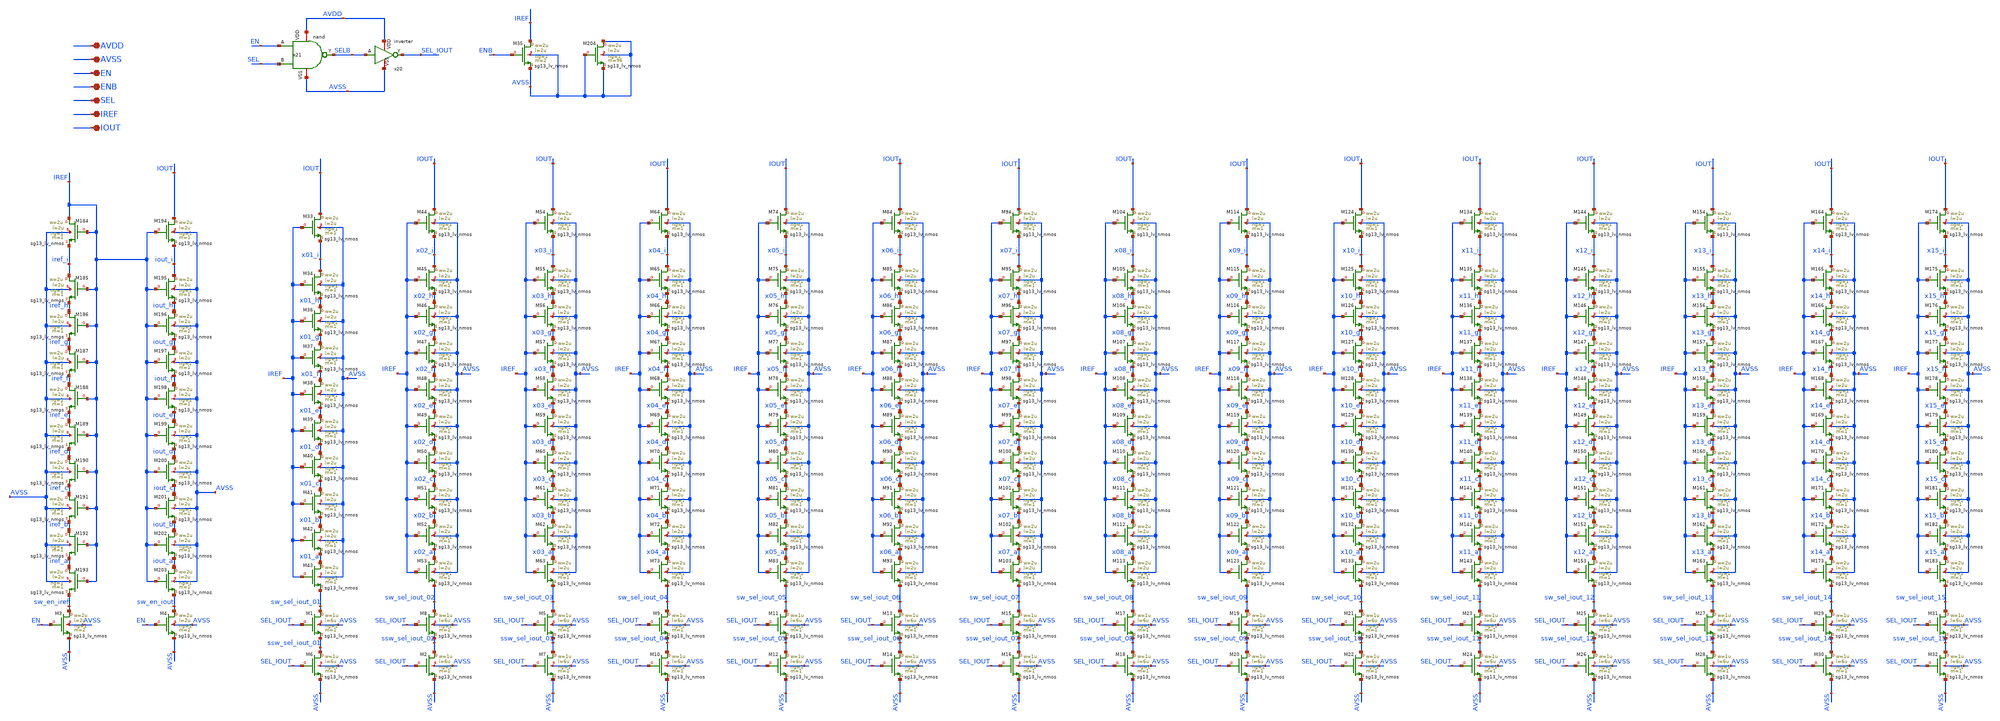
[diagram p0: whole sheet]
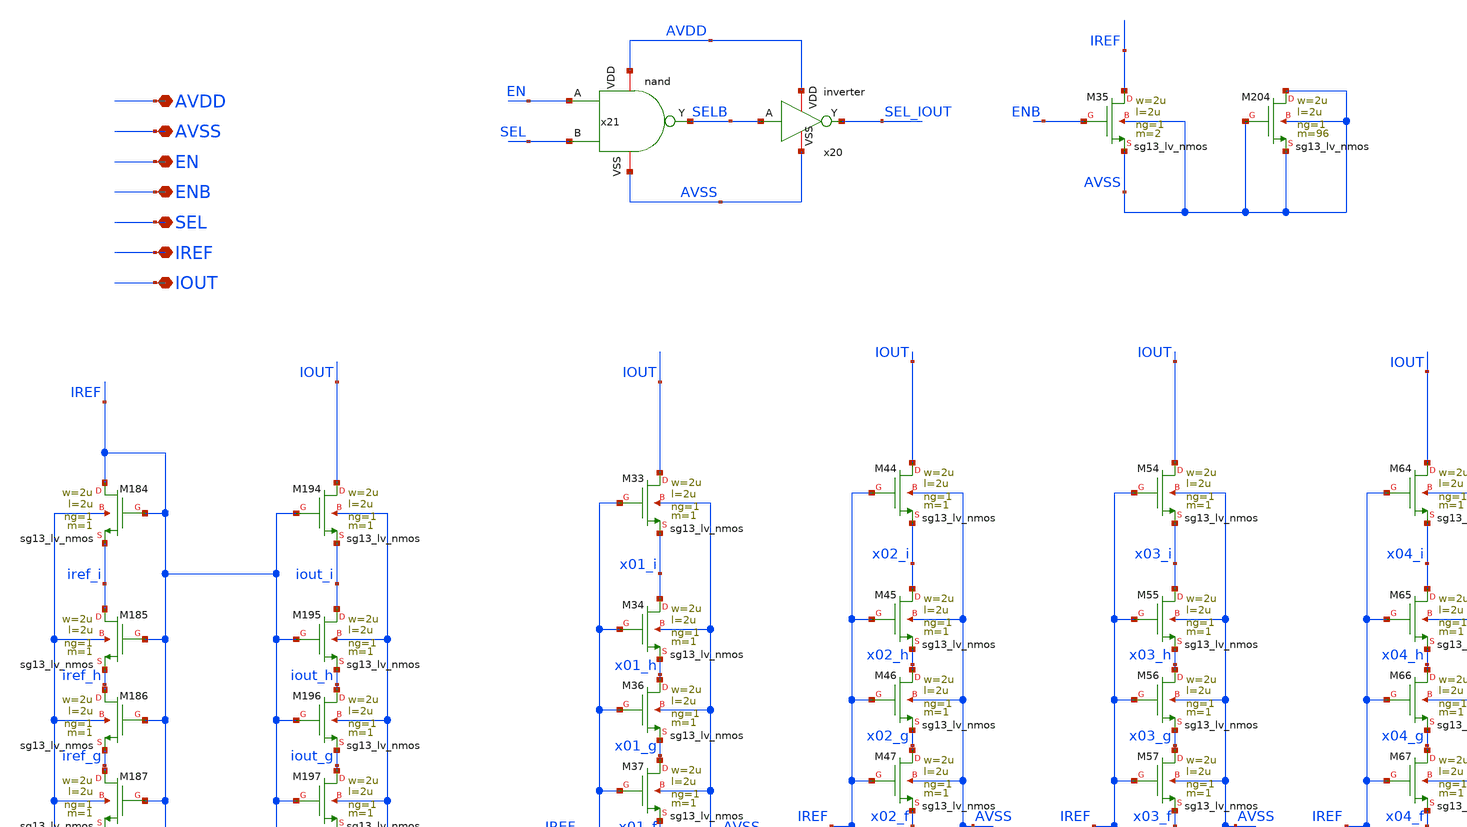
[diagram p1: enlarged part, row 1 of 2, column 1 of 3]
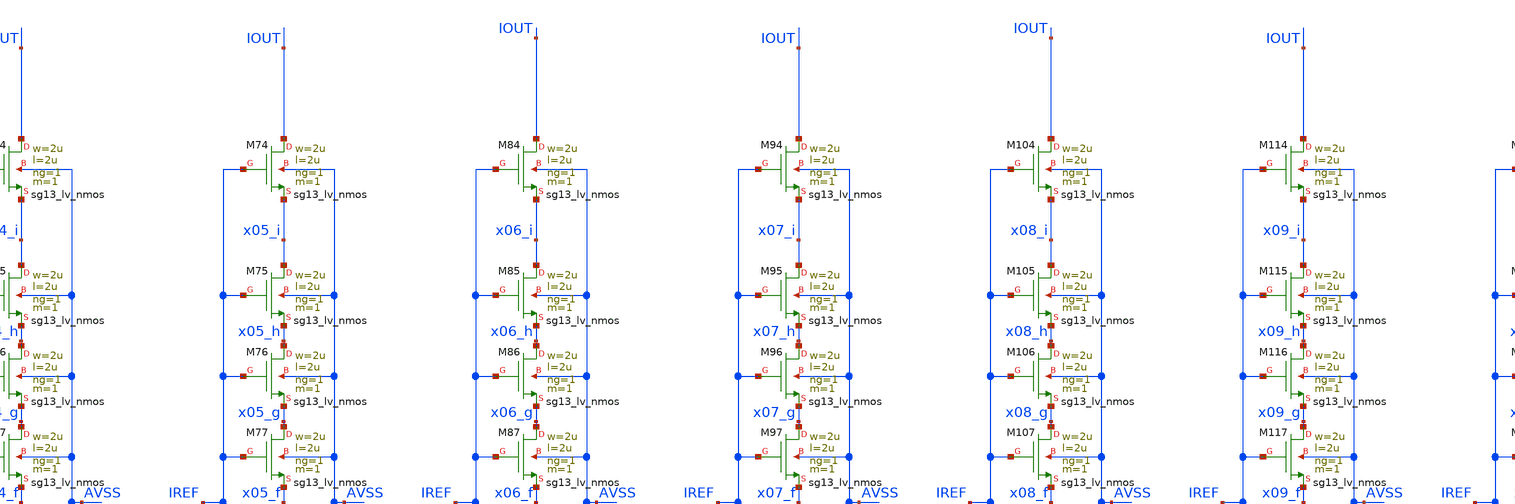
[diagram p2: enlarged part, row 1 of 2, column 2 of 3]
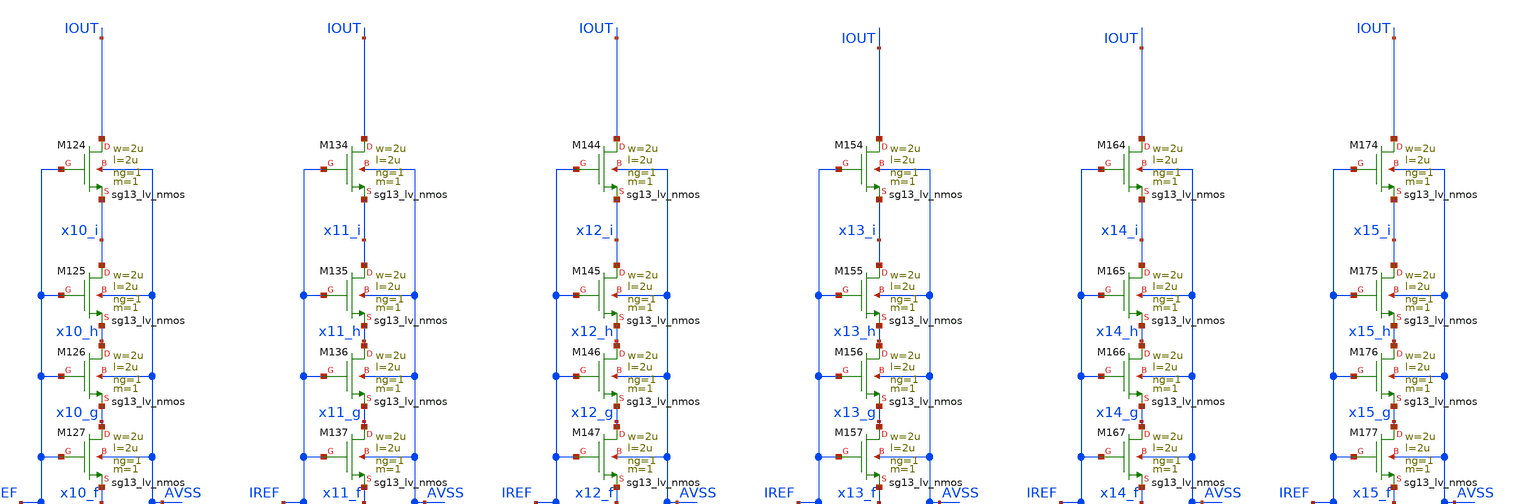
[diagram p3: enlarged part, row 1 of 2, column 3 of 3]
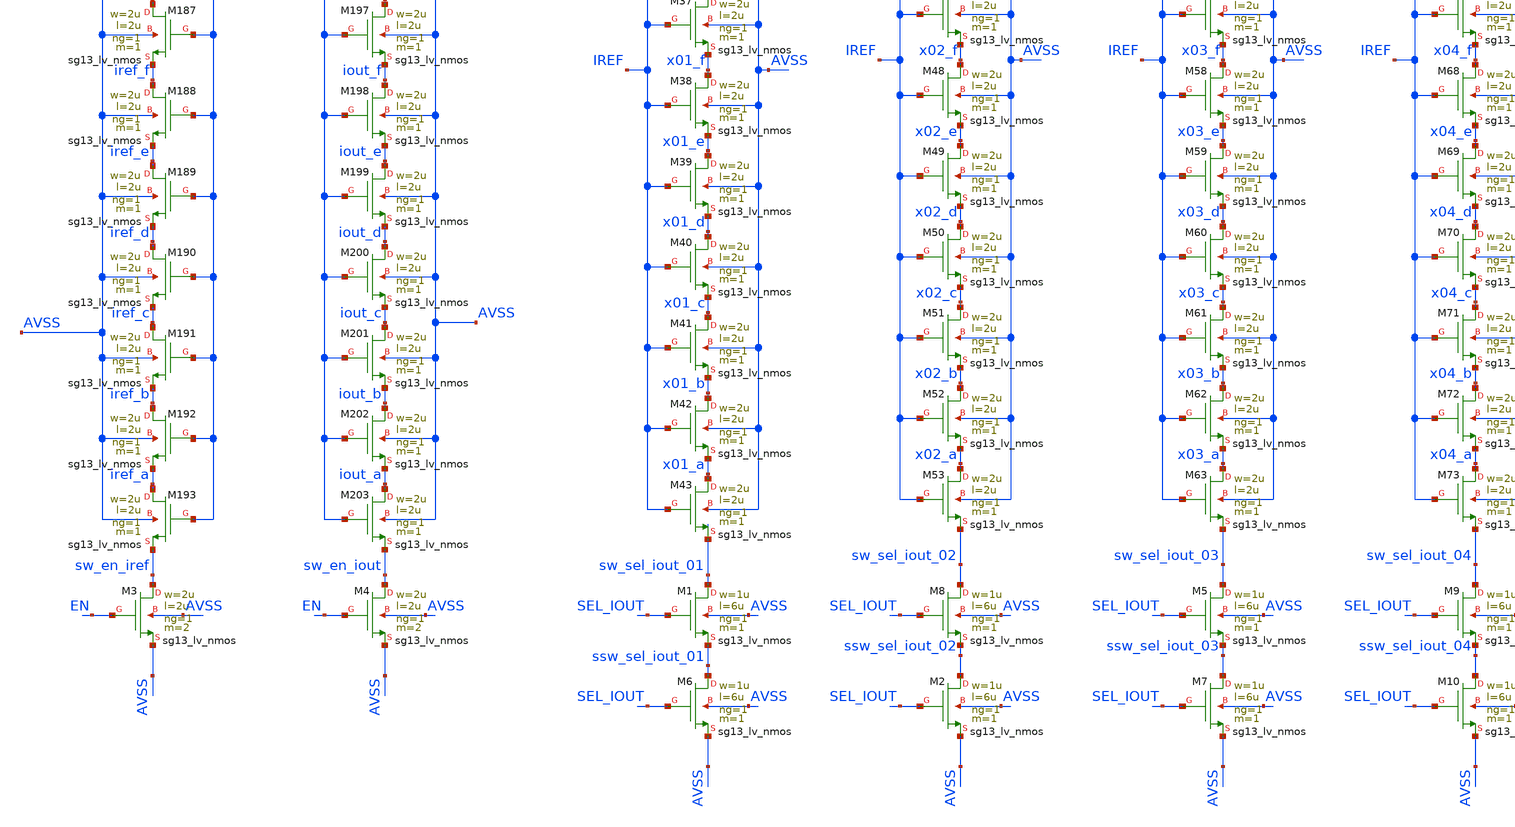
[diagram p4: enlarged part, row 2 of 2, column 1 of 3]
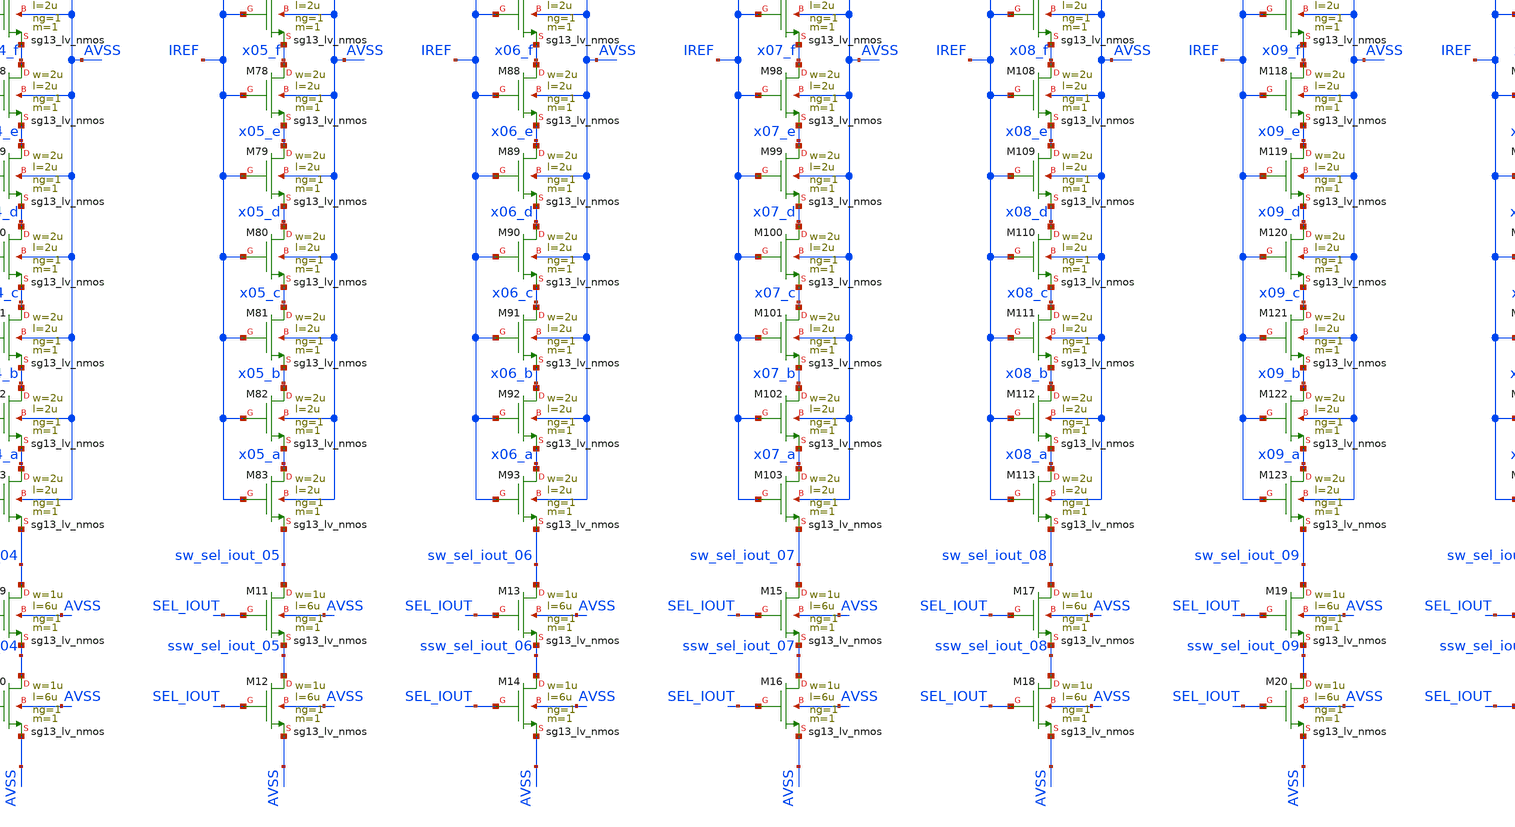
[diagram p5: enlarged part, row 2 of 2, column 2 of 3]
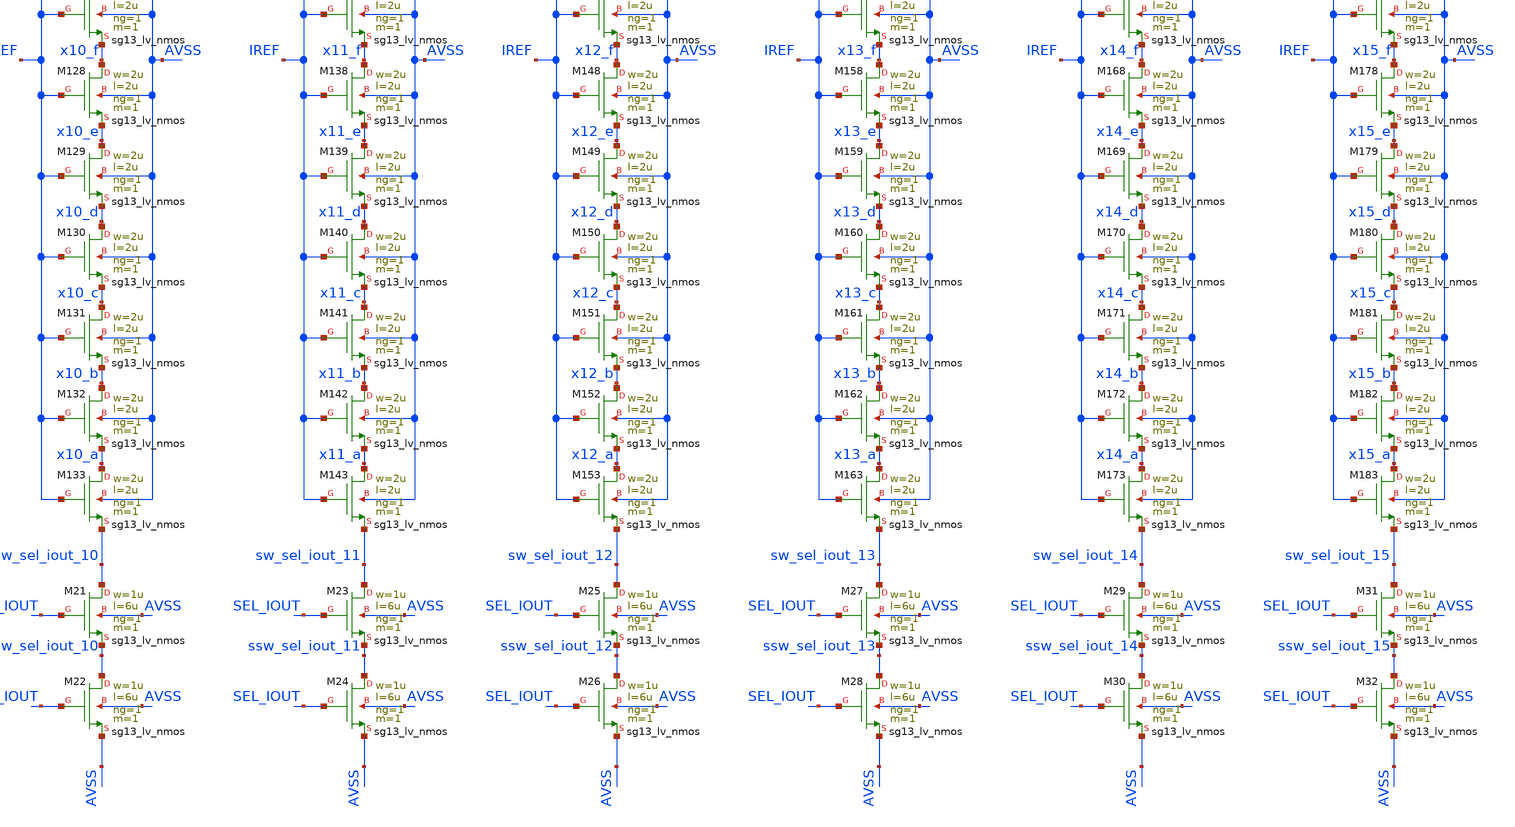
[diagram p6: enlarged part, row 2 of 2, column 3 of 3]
** sch_path: current_generator/analog/DAC/schematics/current_mirror.sch
**.subckt current_mirror AVDD AVSS EN ENB SEL IREF IOUT
*.iopin AVDD
*.iopin AVSS
*.iopin EN
*.iopin ENB
*.iopin SEL
*.iopin IREF
*.iopin IOUT
XM3 sw_en_iref EN AVSS AVSS sg13_lv_nmos w=2u l=2u ng=1 m=2 mm_ok=1
XM4 sw_en_iout EN AVSS AVSS sg13_lv_nmos w=2u l=2u ng=1 m=2 mm_ok=1
XM8 sw_sel_iout_02 SEL_IOUT ssw_sel_iout_02 AVSS sg13_lv_nmos w=1u l=6u ng=1 m=1 mm_ok=1
XM35 IREF ENB AVSS AVSS sg13_lv_nmos w=2u l=2u ng=1 m=2 mm_ok=1
XM2 ssw_sel_iout_02 SEL_IOUT AVSS AVSS sg13_lv_nmos w=1u l=6u ng=1 m=1 mm_ok=1
XM1 sw_sel_iout_01 SEL_IOUT ssw_sel_iout_01 AVSS sg13_lv_nmos w=1u l=6u ng=1 m=1 mm_ok=1
XM6 ssw_sel_iout_01 SEL_IOUT AVSS AVSS sg13_lv_nmos w=1u l=6u ng=1 m=1 mm_ok=1
XM5 sw_sel_iout_03 SEL_IOUT ssw_sel_iout_03 AVSS sg13_lv_nmos w=1u l=6u ng=1 m=1 mm_ok=1
XM7 ssw_sel_iout_03 SEL_IOUT AVSS AVSS sg13_lv_nmos w=1u l=6u ng=1 m=1 mm_ok=1
XM9 sw_sel_iout_04 SEL_IOUT ssw_sel_iout_04 AVSS sg13_lv_nmos w=1u l=6u ng=1 m=1 mm_ok=1
XM10 ssw_sel_iout_04 SEL_IOUT AVSS AVSS sg13_lv_nmos w=1u l=6u ng=1 m=1 mm_ok=1
XM11 sw_sel_iout_05 SEL_IOUT ssw_sel_iout_05 AVSS sg13_lv_nmos w=1u l=6u ng=1 m=1 mm_ok=1
XM12 ssw_sel_iout_05 SEL_IOUT AVSS AVSS sg13_lv_nmos w=1u l=6u ng=1 m=1 mm_ok=1
XM13 sw_sel_iout_06 SEL_IOUT ssw_sel_iout_06 AVSS sg13_lv_nmos w=1u l=6u ng=1 m=1 mm_ok=1
XM14 ssw_sel_iout_06 SEL_IOUT AVSS AVSS sg13_lv_nmos w=1u l=6u ng=1 m=1 mm_ok=1
XM15 sw_sel_iout_07 SEL_IOUT ssw_sel_iout_07 AVSS sg13_lv_nmos w=1u l=6u ng=1 m=1 mm_ok=1
XM16 ssw_sel_iout_07 SEL_IOUT AVSS AVSS sg13_lv_nmos w=1u l=6u ng=1 m=1 mm_ok=1
XM17 sw_sel_iout_08 SEL_IOUT ssw_sel_iout_08 AVSS sg13_lv_nmos w=1u l=6u ng=1 m=1 mm_ok=1
XM18 ssw_sel_iout_08 SEL_IOUT AVSS AVSS sg13_lv_nmos w=1u l=6u ng=1 m=1 mm_ok=1
XM19 sw_sel_iout_09 SEL_IOUT ssw_sel_iout_09 AVSS sg13_lv_nmos w=1u l=6u ng=1 m=1 mm_ok=1
XM20 ssw_sel_iout_09 SEL_IOUT AVSS AVSS sg13_lv_nmos w=1u l=6u ng=1 m=1 mm_ok=1
XM21 sw_sel_iout_10 SEL_IOUT ssw_sel_iout_10 AVSS sg13_lv_nmos w=1u l=6u ng=1 m=1 mm_ok=1
XM22 ssw_sel_iout_10 SEL_IOUT AVSS AVSS sg13_lv_nmos w=1u l=6u ng=1 m=1 mm_ok=1
XM23 sw_sel_iout_11 SEL_IOUT ssw_sel_iout_11 AVSS sg13_lv_nmos w=1u l=6u ng=1 m=1 mm_ok=1
XM24 ssw_sel_iout_11 SEL_IOUT AVSS AVSS sg13_lv_nmos w=1u l=6u ng=1 m=1 mm_ok=1
XM25 sw_sel_iout_12 SEL_IOUT ssw_sel_iout_12 AVSS sg13_lv_nmos w=1u l=6u ng=1 m=1 mm_ok=1
XM26 ssw_sel_iout_12 SEL_IOUT AVSS AVSS sg13_lv_nmos w=1u l=6u ng=1 m=1 mm_ok=1
XM27 sw_sel_iout_13 SEL_IOUT ssw_sel_iout_13 AVSS sg13_lv_nmos w=1u l=6u ng=1 m=1 mm_ok=1
XM28 ssw_sel_iout_13 SEL_IOUT AVSS AVSS sg13_lv_nmos w=1u l=6u ng=1 m=1 mm_ok=1
XM29 sw_sel_iout_14 SEL_IOUT ssw_sel_iout_14 AVSS sg13_lv_nmos w=1u l=6u ng=1 m=1 mm_ok=1
XM30 ssw_sel_iout_14 SEL_IOUT AVSS AVSS sg13_lv_nmos w=1u l=6u ng=1 m=1 mm_ok=1
XM31 sw_sel_iout_15 SEL_IOUT ssw_sel_iout_15 AVSS sg13_lv_nmos w=1u l=6u ng=1 m=1 mm_ok=1
XM32 ssw_sel_iout_15 SEL_IOUT AVSS AVSS sg13_lv_nmos w=1u l=6u ng=1 m=1 mm_ok=1
x20 SELB SEL_IOUT AVDD AVSS inverter
x21 AVDD AVSS EN SEL SELB nand
XM33 IOUT IREF x01_i AVSS sg13_lv_nmos w=2u l=2u ng=1 m=1 mm_ok=1
XM34 x01_i IREF x01_h AVSS sg13_lv_nmos w=2u l=2u ng=1 m=1 mm_ok=1
XM36 x01_h IREF x01_g AVSS sg13_lv_nmos w=2u l=2u ng=1 m=1 mm_ok=1
XM37 x01_g IREF x01_f AVSS sg13_lv_nmos w=2u l=2u ng=1 m=1 mm_ok=1
XM38 x01_f IREF x01_e AVSS sg13_lv_nmos w=2u l=2u ng=1 m=1 mm_ok=1
XM39 x01_e IREF x01_d AVSS sg13_lv_nmos w=2u l=2u ng=1 m=1 mm_ok=1
XM40 x01_d IREF x01_c AVSS sg13_lv_nmos w=2u l=2u ng=1 m=1 mm_ok=1
XM41 x01_c IREF x01_b AVSS sg13_lv_nmos w=2u l=2u ng=1 m=1 mm_ok=1
XM42 x01_b IREF x01_a AVSS sg13_lv_nmos w=2u l=2u ng=1 m=1 mm_ok=1
XM43 x01_a IREF sw_sel_iout_01 AVSS sg13_lv_nmos w=2u l=2u ng=1 m=1 mm_ok=1
XM44 IOUT IREF x02_i AVSS sg13_lv_nmos w=2u l=2u ng=1 m=1 mm_ok=1
XM45 x02_i IREF x02_h AVSS sg13_lv_nmos w=2u l=2u ng=1 m=1 mm_ok=1
XM46 x02_h IREF x02_g AVSS sg13_lv_nmos w=2u l=2u ng=1 m=1 mm_ok=1
XM47 x02_g IREF x02_f AVSS sg13_lv_nmos w=2u l=2u ng=1 m=1 mm_ok=1
XM48 x02_f IREF x02_e AVSS sg13_lv_nmos w=2u l=2u ng=1 m=1 mm_ok=1
XM49 x02_e IREF x02_d AVSS sg13_lv_nmos w=2u l=2u ng=1 m=1 mm_ok=1
XM50 x02_d IREF x02_c AVSS sg13_lv_nmos w=2u l=2u ng=1 m=1 mm_ok=1
XM51 x02_c IREF x02_b AVSS sg13_lv_nmos w=2u l=2u ng=1 m=1 mm_ok=1
XM52 x02_b IREF x02_a AVSS sg13_lv_nmos w=2u l=2u ng=1 m=1 mm_ok=1
XM53 x02_a IREF sw_sel_iout_02 AVSS sg13_lv_nmos w=2u l=2u ng=1 m=1 mm_ok=1
XM54 IOUT IREF x03_i AVSS sg13_lv_nmos w=2u l=2u ng=1 m=1 mm_ok=1
XM55 x03_i IREF x03_h AVSS sg13_lv_nmos w=2u l=2u ng=1 m=1 mm_ok=1
XM56 x03_h IREF x03_g AVSS sg13_lv_nmos w=2u l=2u ng=1 m=1 mm_ok=1
XM57 x03_g IREF x03_f AVSS sg13_lv_nmos w=2u l=2u ng=1 m=1 mm_ok=1
XM58 x03_f IREF x03_e AVSS sg13_lv_nmos w=2u l=2u ng=1 m=1 mm_ok=1
XM59 x03_e IREF x03_d AVSS sg13_lv_nmos w=2u l=2u ng=1 m=1 mm_ok=1
XM60 x03_d IREF x03_c AVSS sg13_lv_nmos w=2u l=2u ng=1 m=1 mm_ok=1
XM61 x03_c IREF x03_b AVSS sg13_lv_nmos w=2u l=2u ng=1 m=1 mm_ok=1
XM62 x03_b IREF x03_a AVSS sg13_lv_nmos w=2u l=2u ng=1 m=1 mm_ok=1
XM63 x03_a IREF sw_sel_iout_03 AVSS sg13_lv_nmos w=2u l=2u ng=1 m=1 mm_ok=1
XM64 IOUT IREF x04_i AVSS sg13_lv_nmos w=2u l=2u ng=1 m=1 mm_ok=1
XM65 x04_i IREF x04_h AVSS sg13_lv_nmos w=2u l=2u ng=1 m=1 mm_ok=1
XM66 x04_h IREF x04_g AVSS sg13_lv_nmos w=2u l=2u ng=1 m=1 mm_ok=1
XM67 x04_g IREF x04_f AVSS sg13_lv_nmos w=2u l=2u ng=1 m=1 mm_ok=1
XM68 x04_f IREF x04_e AVSS sg13_lv_nmos w=2u l=2u ng=1 m=1 mm_ok=1
XM69 x04_e IREF x04_d AVSS sg13_lv_nmos w=2u l=2u ng=1 m=1 mm_ok=1
XM70 x04_d IREF x04_c AVSS sg13_lv_nmos w=2u l=2u ng=1 m=1 mm_ok=1
XM71 x04_c IREF x04_b AVSS sg13_lv_nmos w=2u l=2u ng=1 m=1 mm_ok=1
XM72 x04_b IREF x04_a AVSS sg13_lv_nmos w=2u l=2u ng=1 m=1 mm_ok=1
XM73 x04_a IREF sw_sel_iout_04 AVSS sg13_lv_nmos w=2u l=2u ng=1 m=1 mm_ok=1
XM74 IOUT IREF x05_i AVSS sg13_lv_nmos w=2u l=2u ng=1 m=1 mm_ok=1
XM75 x05_i IREF x05_h AVSS sg13_lv_nmos w=2u l=2u ng=1 m=1 mm_ok=1
XM76 x05_h IREF x05_g AVSS sg13_lv_nmos w=2u l=2u ng=1 m=1 mm_ok=1
XM77 x05_g IREF x05_f AVSS sg13_lv_nmos w=2u l=2u ng=1 m=1 mm_ok=1
XM78 x05_f IREF x05_e AVSS sg13_lv_nmos w=2u l=2u ng=1 m=1 mm_ok=1
XM79 x05_e IREF x05_d AVSS sg13_lv_nmos w=2u l=2u ng=1 m=1 mm_ok=1
XM80 x05_d IREF x05_c AVSS sg13_lv_nmos w=2u l=2u ng=1 m=1 mm_ok=1
XM81 x05_c IREF x05_b AVSS sg13_lv_nmos w=2u l=2u ng=1 m=1 mm_ok=1
XM82 x05_b IREF x05_a AVSS sg13_lv_nmos w=2u l=2u ng=1 m=1 mm_ok=1
XM83 x05_a IREF sw_sel_iout_05 AVSS sg13_lv_nmos w=2u l=2u ng=1 m=1 mm_ok=1
XM84 IOUT IREF x06_i AVSS sg13_lv_nmos w=2u l=2u ng=1 m=1 mm_ok=1
XM85 x06_i IREF x06_h AVSS sg13_lv_nmos w=2u l=2u ng=1 m=1 mm_ok=1
XM86 x06_h IREF x06_g AVSS sg13_lv_nmos w=2u l=2u ng=1 m=1 mm_ok=1
XM87 x06_g IREF x06_f AVSS sg13_lv_nmos w=2u l=2u ng=1 m=1 mm_ok=1
XM88 x06_f IREF x06_e AVSS sg13_lv_nmos w=2u l=2u ng=1 m=1 mm_ok=1
XM89 x06_e IREF x06_d AVSS sg13_lv_nmos w=2u l=2u ng=1 m=1 mm_ok=1
XM90 x06_d IREF x06_c AVSS sg13_lv_nmos w=2u l=2u ng=1 m=1 mm_ok=1
XM91 x06_c IREF x06_b AVSS sg13_lv_nmos w=2u l=2u ng=1 m=1 mm_ok=1
XM92 x06_b IREF x06_a AVSS sg13_lv_nmos w=2u l=2u ng=1 m=1 mm_ok=1
XM93 x06_a IREF sw_sel_iout_06 AVSS sg13_lv_nmos w=2u l=2u ng=1 m=1 mm_ok=1
XM94 IOUT IREF x07_i AVSS sg13_lv_nmos w=2u l=2u ng=1 m=1 mm_ok=1
XM95 x07_i IREF x07_h AVSS sg13_lv_nmos w=2u l=2u ng=1 m=1 mm_ok=1
XM96 x07_h IREF x07_g AVSS sg13_lv_nmos w=2u l=2u ng=1 m=1 mm_ok=1
XM97 x07_g IREF x07_f AVSS sg13_lv_nmos w=2u l=2u ng=1 m=1 mm_ok=1
XM98 x07_f IREF x07_e AVSS sg13_lv_nmos w=2u l=2u ng=1 m=1 mm_ok=1
XM99 x07_e IREF x07_d AVSS sg13_lv_nmos w=2u l=2u ng=1 m=1 mm_ok=1
XM100 x07_d IREF x07_c AVSS sg13_lv_nmos w=2u l=2u ng=1 m=1 mm_ok=1
XM101 x07_c IREF x07_b AVSS sg13_lv_nmos w=2u l=2u ng=1 m=1 mm_ok=1
XM102 x07_b IREF x07_a AVSS sg13_lv_nmos w=2u l=2u ng=1 m=1 mm_ok=1
XM103 x07_a IREF sw_sel_iout_07 AVSS sg13_lv_nmos w=2u l=2u ng=1 m=1 mm_ok=1
XM104 IOUT IREF x08_i AVSS sg13_lv_nmos w=2u l=2u ng=1 m=1 mm_ok=1
XM105 x08_i IREF x08_h AVSS sg13_lv_nmos w=2u l=2u ng=1 m=1 mm_ok=1
XM106 x08_h IREF x08_g AVSS sg13_lv_nmos w=2u l=2u ng=1 m=1 mm_ok=1
XM107 x08_g IREF x08_f AVSS sg13_lv_nmos w=2u l=2u ng=1 m=1 mm_ok=1
XM108 x08_f IREF x08_e AVSS sg13_lv_nmos w=2u l=2u ng=1 m=1 mm_ok=1
XM109 x08_e IREF x08_d AVSS sg13_lv_nmos w=2u l=2u ng=1 m=1 mm_ok=1
XM110 x08_d IREF x08_c AVSS sg13_lv_nmos w=2u l=2u ng=1 m=1 mm_ok=1
XM111 x08_c IREF x08_b AVSS sg13_lv_nmos w=2u l=2u ng=1 m=1 mm_ok=1
XM112 x08_b IREF x08_a AVSS sg13_lv_nmos w=2u l=2u ng=1 m=1 mm_ok=1
XM113 x08_a IREF sw_sel_iout_08 AVSS sg13_lv_nmos w=2u l=2u ng=1 m=1 mm_ok=1
XM114 IOUT IREF x09_i AVSS sg13_lv_nmos w=2u l=2u ng=1 m=1 mm_ok=1
XM115 x09_i IREF x09_h AVSS sg13_lv_nmos w=2u l=2u ng=1 m=1 mm_ok=1
XM116 x09_h IREF x09_g AVSS sg13_lv_nmos w=2u l=2u ng=1 m=1 mm_ok=1
XM117 x09_g IREF x09_f AVSS sg13_lv_nmos w=2u l=2u ng=1 m=1 mm_ok=1
XM118 x09_f IREF x09_e AVSS sg13_lv_nmos w=2u l=2u ng=1 m=1 mm_ok=1
XM119 x09_e IREF x09_d AVSS sg13_lv_nmos w=2u l=2u ng=1 m=1 mm_ok=1
XM120 x09_d IREF x09_c AVSS sg13_lv_nmos w=2u l=2u ng=1 m=1 mm_ok=1
XM121 x09_c IREF x09_b AVSS sg13_lv_nmos w=2u l=2u ng=1 m=1 mm_ok=1
XM122 x09_b IREF x09_a AVSS sg13_lv_nmos w=2u l=2u ng=1 m=1 mm_ok=1
XM123 x09_a IREF sw_sel_iout_09 AVSS sg13_lv_nmos w=2u l=2u ng=1 m=1 mm_ok=1
XM124 IOUT IREF x10_i AVSS sg13_lv_nmos w=2u l=2u ng=1 m=1 mm_ok=1
XM125 x10_i IREF x10_h AVSS sg13_lv_nmos w=2u l=2u ng=1 m=1 mm_ok=1
XM126 x10_h IREF x10_g AVSS sg13_lv_nmos w=2u l=2u ng=1 m=1 mm_ok=1
XM127 x10_g IREF x10_f AVSS sg13_lv_nmos w=2u l=2u ng=1 m=1 mm_ok=1
XM128 x10_f IREF x10_e AVSS sg13_lv_nmos w=2u l=2u ng=1 m=1 mm_ok=1
XM129 x10_e IREF x10_d AVSS sg13_lv_nmos w=2u l=2u ng=1 m=1 mm_ok=1
XM130 x10_d IREF x10_c AVSS sg13_lv_nmos w=2u l=2u ng=1 m=1 mm_ok=1
XM131 x10_c IREF x10_b AVSS sg13_lv_nmos w=2u l=2u ng=1 m=1 mm_ok=1
XM132 x10_b IREF x10_a AVSS sg13_lv_nmos w=2u l=2u ng=1 m=1 mm_ok=1
XM133 x10_a IREF sw_sel_iout_10 AVSS sg13_lv_nmos w=2u l=2u ng=1 m=1 mm_ok=1
XM134 IOUT IREF x11_i AVSS sg13_lv_nmos w=2u l=2u ng=1 m=1 mm_ok=1
XM135 x11_i IREF x11_h AVSS sg13_lv_nmos w=2u l=2u ng=1 m=1 mm_ok=1
XM136 x11_h IREF x11_g AVSS sg13_lv_nmos w=2u l=2u ng=1 m=1 mm_ok=1
XM137 x11_g IREF x11_f AVSS sg13_lv_nmos w=2u l=2u ng=1 m=1 mm_ok=1
XM138 x11_f IREF x11_e AVSS sg13_lv_nmos w=2u l=2u ng=1 m=1 mm_ok=1
XM139 x11_e IREF x11_d AVSS sg13_lv_nmos w=2u l=2u ng=1 m=1 mm_ok=1
XM140 x11_d IREF x11_c AVSS sg13_lv_nmos w=2u l=2u ng=1 m=1 mm_ok=1
XM141 x11_c IREF x11_b AVSS sg13_lv_nmos w=2u l=2u ng=1 m=1 mm_ok=1
XM142 x11_b IREF x11_a AVSS sg13_lv_nmos w=2u l=2u ng=1 m=1 mm_ok=1
XM143 x11_a IREF sw_sel_iout_11 AVSS sg13_lv_nmos w=2u l=2u ng=1 m=1 mm_ok=1
XM144 IOUT IREF x12_i AVSS sg13_lv_nmos w=2u l=2u ng=1 m=1 mm_ok=1
XM145 x12_i IREF x12_h AVSS sg13_lv_nmos w=2u l=2u ng=1 m=1 mm_ok=1
XM146 x12_h IREF x12_g AVSS sg13_lv_nmos w=2u l=2u ng=1 m=1 mm_ok=1
XM147 x12_g IREF x12_f AVSS sg13_lv_nmos w=2u l=2u ng=1 m=1 mm_ok=1
XM148 x12_f IREF x12_e AVSS sg13_lv_nmos w=2u l=2u ng=1 m=1 mm_ok=1
XM149 x12_e IREF x12_d AVSS sg13_lv_nmos w=2u l=2u ng=1 m=1 mm_ok=1
XM150 x12_d IREF x12_c AVSS sg13_lv_nmos w=2u l=2u ng=1 m=1 mm_ok=1
XM151 x12_c IREF x12_b AVSS sg13_lv_nmos w=2u l=2u ng=1 m=1 mm_ok=1
XM152 x12_b IREF x12_a AVSS sg13_lv_nmos w=2u l=2u ng=1 m=1 mm_ok=1
XM153 x12_a IREF sw_sel_iout_12 AVSS sg13_lv_nmos w=2u l=2u ng=1 m=1 mm_ok=1
XM154 IOUT IREF x13_i AVSS sg13_lv_nmos w=2u l=2u ng=1 m=1 mm_ok=1
XM155 x13_i IREF x13_h AVSS sg13_lv_nmos w=2u l=2u ng=1 m=1 mm_ok=1
XM156 x13_h IREF x13_g AVSS sg13_lv_nmos w=2u l=2u ng=1 m=1 mm_ok=1
XM157 x13_g IREF x13_f AVSS sg13_lv_nmos w=2u l=2u ng=1 m=1 mm_ok=1
XM158 x13_f IREF x13_e AVSS sg13_lv_nmos w=2u l=2u ng=1 m=1 mm_ok=1
XM159 x13_e IREF x13_d AVSS sg13_lv_nmos w=2u l=2u ng=1 m=1 mm_ok=1
XM160 x13_d IREF x13_c AVSS sg13_lv_nmos w=2u l=2u ng=1 m=1 mm_ok=1
XM161 x13_c IREF x13_b AVSS sg13_lv_nmos w=2u l=2u ng=1 m=1 mm_ok=1
XM162 x13_b IREF x13_a AVSS sg13_lv_nmos w=2u l=2u ng=1 m=1 mm_ok=1
XM163 x13_a IREF sw_sel_iout_13 AVSS sg13_lv_nmos w=2u l=2u ng=1 m=1 mm_ok=1
XM164 IOUT IREF x14_i AVSS sg13_lv_nmos w=2u l=2u ng=1 m=1 mm_ok=1
XM165 x14_i IREF x14_h AVSS sg13_lv_nmos w=2u l=2u ng=1 m=1 mm_ok=1
XM166 x14_h IREF x14_g AVSS sg13_lv_nmos w=2u l=2u ng=1 m=1 mm_ok=1
XM167 x14_g IREF x14_f AVSS sg13_lv_nmos w=2u l=2u ng=1 m=1 mm_ok=1
XM168 x14_f IREF x14_e AVSS sg13_lv_nmos w=2u l=2u ng=1 m=1 mm_ok=1
XM169 x14_e IREF x14_d AVSS sg13_lv_nmos w=2u l=2u ng=1 m=1 mm_ok=1
XM170 x14_d IREF x14_c AVSS sg13_lv_nmos w=2u l=2u ng=1 m=1 mm_ok=1
XM171 x14_c IREF x14_b AVSS sg13_lv_nmos w=2u l=2u ng=1 m=1 mm_ok=1
XM172 x14_b IREF x14_a AVSS sg13_lv_nmos w=2u l=2u ng=1 m=1 mm_ok=1
XM173 x14_a IREF sw_sel_iout_14 AVSS sg13_lv_nmos w=2u l=2u ng=1 m=1 mm_ok=1
XM174 IOUT IREF x15_i AVSS sg13_lv_nmos w=2u l=2u ng=1 m=1 mm_ok=1
XM175 x15_i IREF x15_h AVSS sg13_lv_nmos w=2u l=2u ng=1 m=1 mm_ok=1
XM176 x15_h IREF x15_g AVSS sg13_lv_nmos w=2u l=2u ng=1 m=1 mm_ok=1
XM177 x15_g IREF x15_f AVSS sg13_lv_nmos w=2u l=2u ng=1 m=1 mm_ok=1
XM178 x15_f IREF x15_e AVSS sg13_lv_nmos w=2u l=2u ng=1 m=1 mm_ok=1
XM179 x15_e IREF x15_d AVSS sg13_lv_nmos w=2u l=2u ng=1 m=1 mm_ok=1
XM180 x15_d IREF x15_c AVSS sg13_lv_nmos w=2u l=2u ng=1 m=1 mm_ok=1
XM181 x15_c IREF x15_b AVSS sg13_lv_nmos w=2u l=2u ng=1 m=1 mm_ok=1
XM182 x15_b IREF x15_a AVSS sg13_lv_nmos w=2u l=2u ng=1 m=1 mm_ok=1
XM183 x15_a IREF sw_sel_iout_15 AVSS sg13_lv_nmos w=2u l=2u ng=1 m=1 mm_ok=1
XM184 IREF IREF iref_i AVSS sg13_lv_nmos w=2u l=2u ng=1 m=1 mm_ok=1
XM185 iref_i IREF iref_h AVSS sg13_lv_nmos w=2u l=2u ng=1 m=1 mm_ok=1
XM186 iref_h IREF iref_g AVSS sg13_lv_nmos w=2u l=2u ng=1 m=1 mm_ok=1
XM187 iref_g IREF iref_f AVSS sg13_lv_nmos w=2u l=2u ng=1 m=1 mm_ok=1
XM188 iref_f IREF iref_e AVSS sg13_lv_nmos w=2u l=2u ng=1 m=1 mm_ok=1
XM189 iref_e IREF iref_d AVSS sg13_lv_nmos w=2u l=2u ng=1 m=1 mm_ok=1
XM190 iref_d IREF iref_c AVSS sg13_lv_nmos w=2u l=2u ng=1 m=1 mm_ok=1
XM191 iref_c IREF iref_b AVSS sg13_lv_nmos w=2u l=2u ng=1 m=1 mm_ok=1
XM192 iref_b IREF iref_a AVSS sg13_lv_nmos w=2u l=2u ng=1 m=1 mm_ok=1
XM193 iref_a IREF sw_en_iref AVSS sg13_lv_nmos w=2u l=2u ng=1 m=1 mm_ok=1
XM194 IOUT IREF iout_i AVSS sg13_lv_nmos w=2u l=2u ng=1 m=1 mm_ok=1
XM195 iout_i IREF iout_h AVSS sg13_lv_nmos w=2u l=2u ng=1 m=1 mm_ok=1
XM196 iout_h IREF iout_g AVSS sg13_lv_nmos w=2u l=2u ng=1 m=1 mm_ok=1
XM197 iout_g IREF iout_f AVSS sg13_lv_nmos w=2u l=2u ng=1 m=1 mm_ok=1
XM198 iout_f IREF iout_e AVSS sg13_lv_nmos w=2u l=2u ng=1 m=1 mm_ok=1
XM199 iout_e IREF iout_d AVSS sg13_lv_nmos w=2u l=2u ng=1 m=1 mm_ok=1
XM200 iout_d IREF iout_c AVSS sg13_lv_nmos w=2u l=2u ng=1 m=1 mm_ok=1
XM201 iout_c IREF iout_b AVSS sg13_lv_nmos w=2u l=2u ng=1 m=1 mm_ok=1
XM202 iout_b IREF iout_a AVSS sg13_lv_nmos w=2u l=2u ng=1 m=1 mm_ok=1
XM203 iout_a IREF sw_en_iout AVSS sg13_lv_nmos w=2u l=2u ng=1 m=1 mm_ok=1
XM204 AVSS AVSS AVSS AVSS sg13_lv_nmos w=2u l=2u ng=1 m=96 mm_ok=1
**.ends

* expanding   symbol:  inverter.sym # of pins=4
** sym_path: current_generator/analog/DAC/schematics/inverter.sym
** sch_path: current_generator/analog/DAC/schematics/inverter.sch
.subckt inverter A Y VDD VSS
*.opin Y
*.ipin A
*.iopin VDD
*.iopin VSS
MMN0 Y A VSS VSS sg13_lv_nmos w=740.00n l=130.00n ng=1 m=1 mm_ok=1
MMP0 Y A VDD VDD sg13_lv_pmos w=1.12u l=130.00n ng=1 m=1 mm_ok=1
.ends


* expanding   symbol:  nand.sym # of pins=5
** sym_path: current_generator/analog/DAC/schematics/nand.sym
** sch_path: current_generator/analog/DAC/schematics/nand.sch
.subckt nand VDD VSS A B Y
*.opin Y
*.ipin A
*.iopin VDD
*.iopin VSS
*.ipin B
XMN0 net1 B VSS VSS sg13_lv_nmos w=1.44u l=130.00n ng=2 m=1 mm_ok=1
XMP0 Y B VDD VDD sg13_lv_pmos w=2.24u l=130.00n ng=2 m=1 mm_ok=1
XMN1 Y A net1 VSS sg13_lv_nmos w=1.44u l=130.00n ng=2 m=1 mm_ok=1
XMP1 Y A VDD VDD sg13_lv_pmos w=2.24u l=130.00n ng=2 m=1 mm_ok=1
.ends

.end
